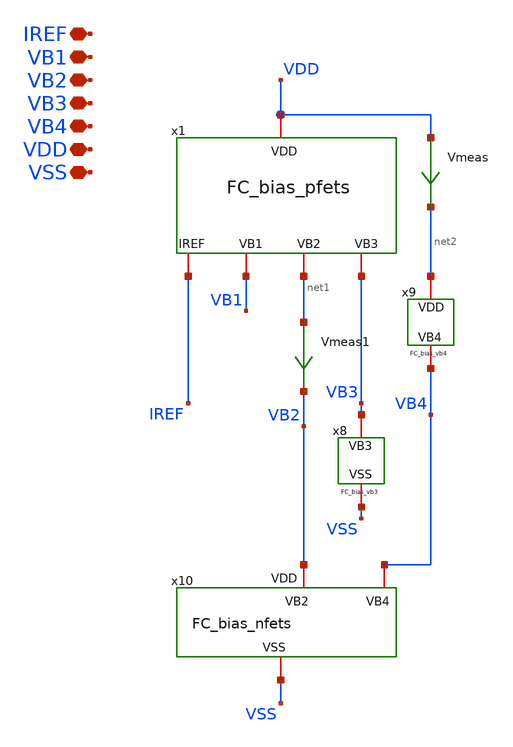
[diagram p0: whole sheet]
** sch_path: TIA_Filter/Folded/FC_bias_net.sch
**.subckt FC_bias_net VDD VSS VB2 IREF VB3 VB4 VB1
*.iopin VDD
*.iopin VSS
*.iopin VB2
*.iopin IREF
*.iopin VB3
*.iopin VB4
*.iopin VB1
x8 VB3 VSS FC_bias_vb3
x9 VB4 net2 FC_bias_vb4
x10 VB2 VB4 VSS FC_bias_nfets
x1 VB1 net1 VB3 IREF VDD FC_bias_pfets
Vmeas VDD net2 0
.save i(vmeas)
Vmeas1 net1 VB2 0
.save i(vmeas1)
**.ends
.end
